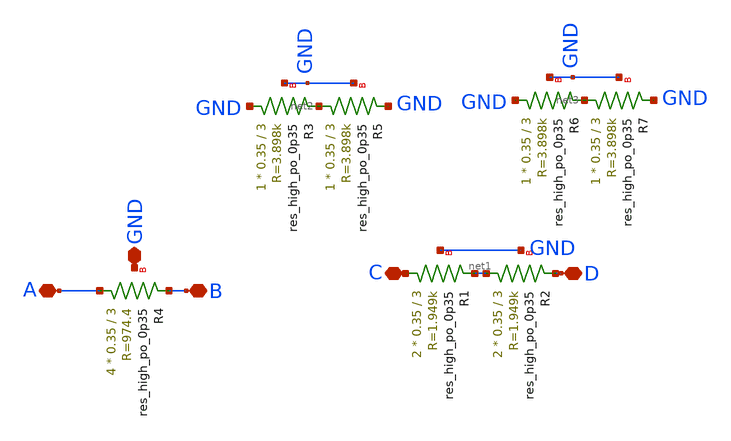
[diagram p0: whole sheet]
** sch_path: magic/resistor_op_tt.sch
**.subckt resistor_op_tt GND C D A B
*.iopin GND
*.iopin C
*.iopin D
*.iopin A
*.iopin B
XR4 A B GND sky130_fd_pr__res_high_po_0p35 L=3 mult=4 m=4
XR1 C net1 GND sky130_fd_pr__res_high_po_0p35 L=3 mult=2 m=2
XR2 net1 D GND sky130_fd_pr__res_high_po_0p35 L=3 mult=2 m=2
XR3 GND net2 GND sky130_fd_pr__res_high_po_0p35 L=3 mult=1 m=1
XR5 net2 GND GND sky130_fd_pr__res_high_po_0p35 L=3 mult=1 m=1
XR6 GND net3 GND sky130_fd_pr__res_high_po_0p35 L=3 mult=1 m=1
XR7 net3 GND GND sky130_fd_pr__res_high_po_0p35 L=3 mult=1 m=1
**.ends
.end
